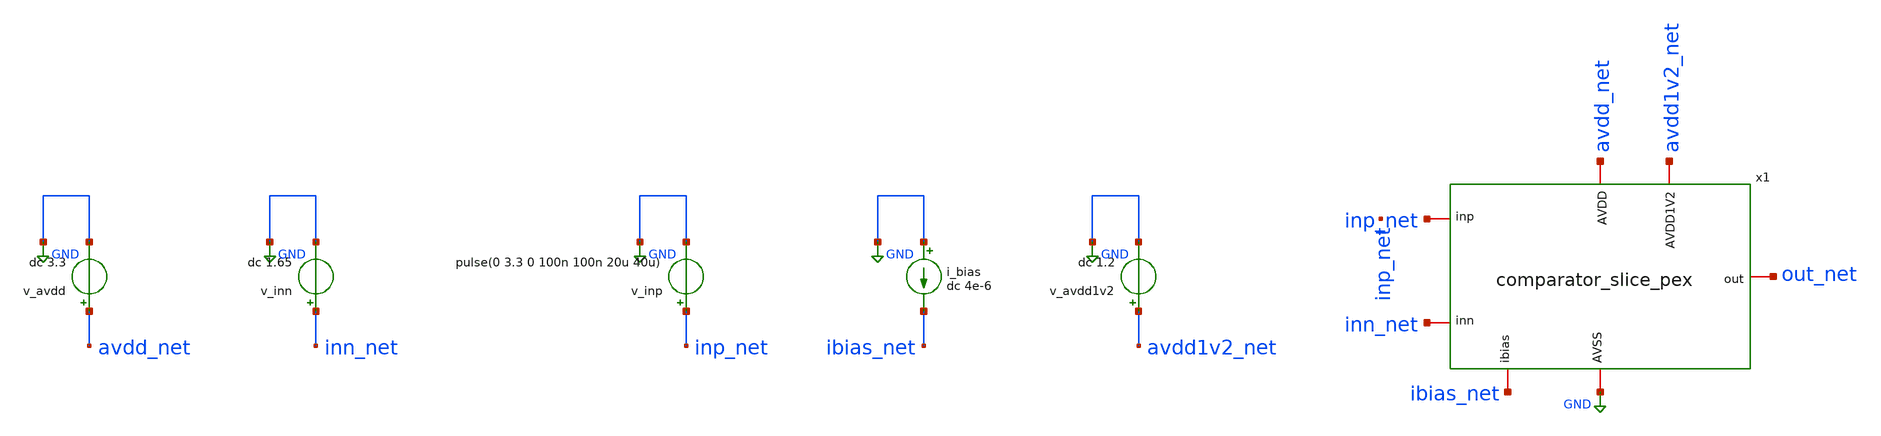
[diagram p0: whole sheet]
** sch_path: macros/comparator/testbenches/xschem/tb_comparator_slice_pex.sch
**.subckt tb_comparator_slice_pex
v_avdd avdd_net GND dc 3.3
v_inn inn_net GND dc 1.65
v_inp inp_net GND pulse(0 3.3 0 100n 100n 20u 40u)
i_bias GND ibias_net dc 4e-6
v_avdd1v2 avdd1v2_net GND dc 1.2
x1 inp_net inn_net ibias_net out_net avdd_net GND avdd1v2_net comparator_slice_pex
**** begin user architecture code


.lib $PDK_ROOT/$PDK/libs.tech/ngspice/models/cornerMOShv.lib mos_tt
.lib $PDK_ROOT/$PDK/libs.tech/ngspice/models/cornerRES.lib res_typ
.include ../../../netlist/pex/comparator_slice_magic_pex_3.spice




.op
.tran 100n 100u
.control
  run
  plot v(out_net) v(inp_net) v(inn_net)
.endc


**** end user architecture code
**.ends
.GLOBAL GND
.end
